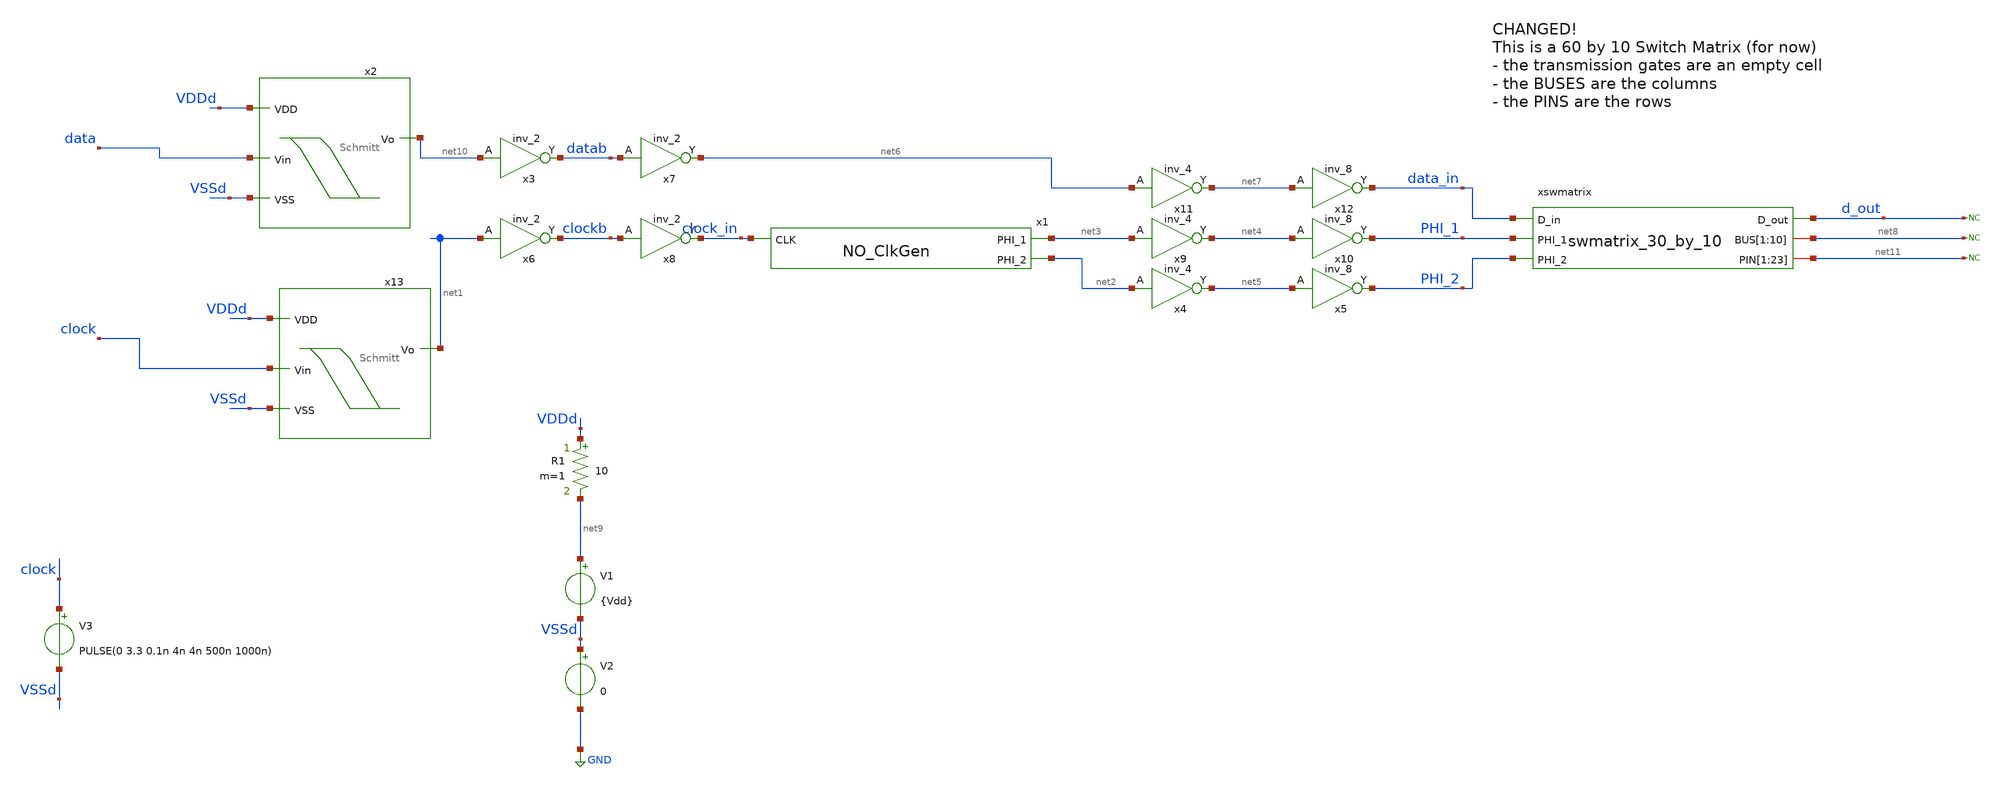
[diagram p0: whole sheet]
** sch_path: designs/switch_matrix_gf180mcu_9t5v0-main/designs/Swmatrix.sch
**.subckt Swmatrix
x1 net2 clock_in net3 NO_ClkGen
xswmatrix data_in d_out PHI_1 PHI_2 net8 net8 net8 net8 net8 net8 net8 net8 net8 net8 net11 net11
+ net11 net11 net11 net11 net11 net11 net11 net11 net11 net11 net11 net11 net11 net11 net11 net11 net11
+ net11 net11 net11 net11 swmatrix_30_by_10
V1 net9 VSSd {Vdd}
V2 VSSd GND 0
x3 net10 VSSd VDDd VSSd VDDd datab gf180mcu_fd_sc_mcu9t5v0__inv_2
x4 net2 VSSd VDDd VSSd VDDd net5 gf180mcu_fd_sc_mcu9t5v0__inv_4
x5 net5 VSSd VDDd VSSd VDDd PHI_2 gf180mcu_fd_sc_mcu9t5v0__inv_8
x6 net1 VSSd VDDd VSSd VDDd clockb gf180mcu_fd_sc_mcu9t5v0__inv_2
x7 datab VSSd VDDd VSSd VDDd net6 gf180mcu_fd_sc_mcu9t5v0__inv_2
x8 clockb VSSd VDDd VSSd VDDd clock_in gf180mcu_fd_sc_mcu9t5v0__inv_2
x9 net3 VSSd VDDd VSSd VDDd net4 gf180mcu_fd_sc_mcu9t5v0__inv_4
x10 net4 VSSd VDDd VSSd VDDd PHI_1 gf180mcu_fd_sc_mcu9t5v0__inv_8
x11 net6 VSSd VDDd VSSd VDDd net7 gf180mcu_fd_sc_mcu9t5v0__inv_4
x12 net7 VSSd VDDd VSSd VDDd data_in gf180mcu_fd_sc_mcu9t5v0__inv_8
* noconn d_out
* noconn #net8
R1 VDDd net9 10 m=1
* noconn #net11
V3 clock VSSd PULSE(0 3.3 0.1n 4n 4n 500n 1000n)
x2 VDDd data net10 VSSd Schmitt
x13 VDDd clock net1 VSSd Schmitt
**** begin user architecture code

.include /foss/pdks/gf180mcuD/libs.ref/gf180mcu_fd_sc_mcu9t5v0/spice/gf180mcu_fd_sc_mcu9t5v0.spice
.include $::180MCU_MODELS/design.ngspice
.lib $::180MCU_MODELS/sm141064.ngspice typical



.control

    save all
    TRAN 1000n 231000n
    write Swmatrix.raw

.endc




.param VDD = 3.3

.global VDDd VSSd

* data
aclock [ clock_node ] clock_vector
.model clock_vector d_source(input_file="/foss/designs/libs/data_source/data_swmatrix5_10.txt")
* convert digital signals to analog
aconvert [ clock_node ] [  data ] dac_in
.model dac_in dac_bridge (out_low=0V out_high=3.3V t_rise=4ns t_fall=4ns)


**** end user architecture code
**.ends
.GLOBAL GND
.end
